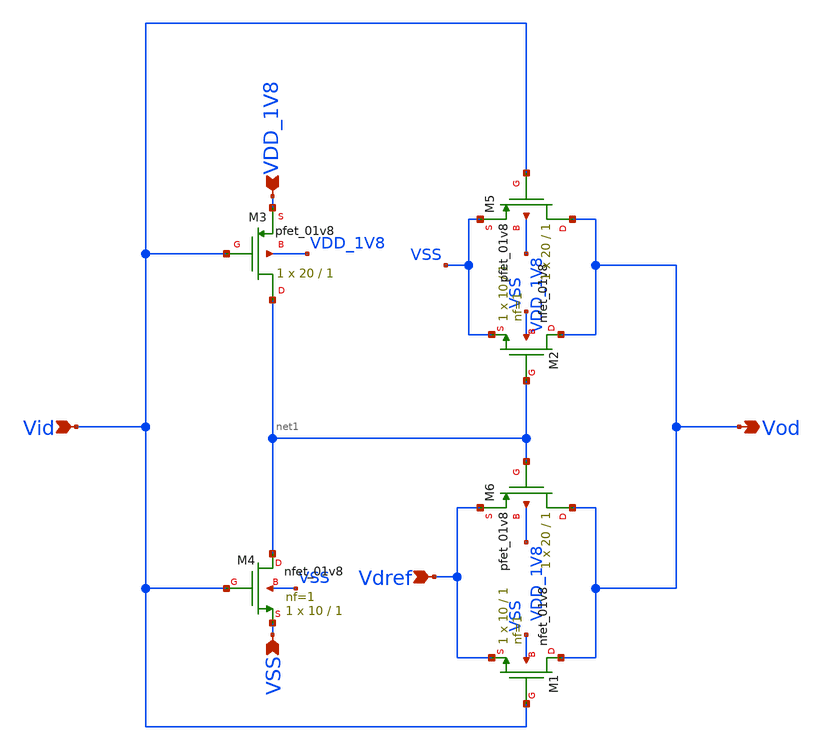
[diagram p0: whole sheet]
** sch_path: design/CNR_GR06_SKY130NM/dac_n.sch
**.subckt dac_n VDD_1V8 VSS Vid Vod Vdref
*.ipin VDD_1V8
*.ipin VSS
*.ipin Vid
*.opin Vod
*.ipin Vdref
XM3 net1 Vid VDD_1V8 VDD_1V8 sky130_fd_pr__pfet_01v8 W=20 L=1 ad='int((nf+1)/2) * W/nf * 0.29' pd='2*int((nf+1)/2) * (W/nf + 0.29)'
+ as='int((nf+2)/2) * W/nf * 0.29' ps='2*int((nf+2)/2) * (W/nf + 0.29)' nrd='0.29 / W' nrs='0.29 / W' sa=0
+ sb=0 sd=0 nf=1 mult=1
XM4 net1 Vid VSS VSS sky130_fd_pr__nfet_01v8 L=1 W=10 nf=1 ad='int((nf+1)/2) * W/nf * 0.29' as='int((nf+2)/2) * W/nf * 0.29'
+ pd='2*int((nf+1)/2) * (W/nf + 0.29)' ps='2*int((nf+2)/2) * (W/nf + 0.29)' nrd='0.29 / W' nrs='0.29 / W'
+ sa=0 sb=0 sd=0 mult=1 m=1
XM1 Vod Vid Vdref VSS sky130_fd_pr__nfet_01v8 L=1 W=10 nf=1 ad='int((nf+1)/2) * W/nf * 0.29' as='int((nf+2)/2) * W/nf * 0.29'
+ pd='2*int((nf+1)/2) * (W/nf + 0.29)' ps='2*int((nf+2)/2) * (W/nf + 0.29)' nrd='0.29 / W' nrs='0.29 / W'
+ sa=0 sb=0 sd=0 mult=1 m=1
XM2 Vod net1 VSS VSS sky130_fd_pr__nfet_01v8 L=1 W=10 nf=1 ad='int((nf+1)/2) * W/nf * 0.29' as='int((nf+2)/2) * W/nf * 0.29'
+ pd='2*int((nf+1)/2) * (W/nf + 0.29)' ps='2*int((nf+2)/2) * (W/nf + 0.29)' nrd='0.29 / W' nrs='0.29 / W'
+ sa=0 sb=0 sd=0 mult=1 m=1
XM5 Vod Vid VSS VDD_1V8 sky130_fd_pr__pfet_01v8 W=20 L=1 ad='int((nf+1)/2) * W/nf * 0.29' pd='2*int((nf+1)/2) * (W/nf + 0.29)'
+ as='int((nf+2)/2) * W/nf * 0.29' ps='2*int((nf+2)/2) * (W/nf + 0.29)' nrd='0.29 / W' nrs='0.29 / W' sa=0
+ sb=0 sd=0 nf=1 mult=1
XM6 Vod net1 Vdref VDD_1V8 sky130_fd_pr__pfet_01v8 W=20 L=1 ad='int((nf+1)/2) * W/nf * 0.29' pd='2*int((nf+1)/2) * (W/nf + 0.29)'
+ as='int((nf+2)/2) * W/nf * 0.29' ps='2*int((nf+2)/2) * (W/nf + 0.29)' nrd='0.29 / W' nrs='0.29 / W' sa=0
+ sb=0 sd=0 nf=1 mult=1
**.ends
.end
